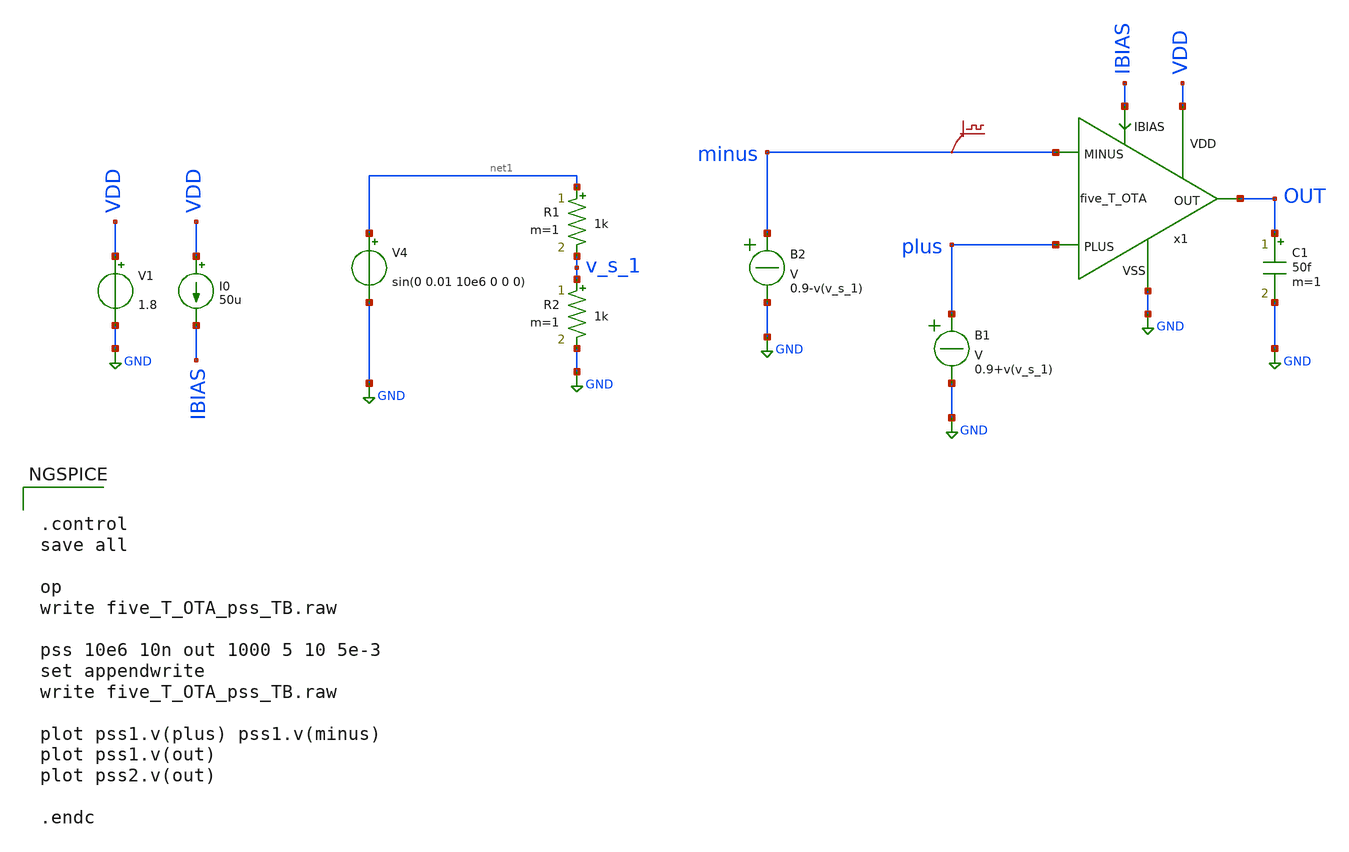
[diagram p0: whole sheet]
** sch_path: examples/xschem/five_T_OTA_pss_TB_2.sch
**.subckt five_T_OTA_pss_TB_2
x1 OUT minus plus IBIAS GND VDD five_T_OTA
V1 VDD GND 1.8
I0 VDD IBIAS 50u
C1 OUT GND 50f m=1
V4 net1 GND sin(0 0.01 10e6 0 0 0)
B1 plus GND V = 0.9+v(v_s_1)
R1 net1 v_s_1 1k m=1
R2 v_s_1 GND 1k m=1
B2 minus GND V = 0.9-v(v_s_1)
.save v(minus)
**** begin user architecture code


.control
save all

op
write five_T_OTA_pss_TB.raw

pss 10e6 10n out 1000 5 10 5e-3
set appendwrite
write five_T_OTA_pss_TB.raw

plot pss1.v(plus) pss1.v(minus)
plot pss1.v(out)
plot pss2.v(out)

.endc



** opencircuitdesign pdks install
.lib $::SKYWATER_MODELS/sky130.lib.spice tt


**** end user architecture code
**.ends

* expanding   symbol:  five_T_OTA.sym # of pins=6
** sym_path: examples/xschem/five_T_OTA.sym
** sch_path: examples/xschem/five_T_OTA.sch
.subckt five_T_OTA OUT MINUS PLUS IBIAS VSS VDD
*.iopin VDD
*.iopin VSS
*.iopin MINUS
*.iopin PLUS
*.iopin OUT
*.iopin IBIAS
XM2 IBIAS IBIAS VSS VSS sky130_fd_pr__nfet_01v8 L=0.3 W=3 nf=1 ad='int((nf+1)/2) * W/nf * 0.29' as='int((nf+2)/2) * W/nf * 0.29'
+ pd='2*int((nf+1)/2) * (W/nf + 0.29)' ps='2*int((nf+2)/2) * (W/nf + 0.29)' nrd='0.29 / W' nrs='0.29 / W'
+ sa=0 sb=0 sd=0 mult=1 m=1
XM1 net1 IBIAS VSS VSS sky130_fd_pr__nfet_01v8 L=0.3 W=3 nf=1 ad='int((nf+1)/2) * W/nf * 0.29' as='int((nf+2)/2) * W/nf * 0.29'
+ pd='2*int((nf+1)/2) * (W/nf + 0.29)' ps='2*int((nf+2)/2) * (W/nf + 0.29)' nrd='0.29 / W' nrs='0.29 / W'
+ sa=0 sb=0 sd=0 mult=4 m=4
.save v(ibias)
.save v(out)
.save v(net2)
.save v(net1)
XM4 net2 PLUS net1 VSS sky130_fd_pr__nfet_01v8_lvt L=0.3 W=4 nf=1 ad='int((nf+1)/2) * W/nf * 0.29' as='int((nf+2)/2) * W/nf * 0.29'
+ pd='2*int((nf+1)/2) * (W/nf + 0.29)' ps='2*int((nf+2)/2) * (W/nf + 0.29)' nrd='0.29 / W' nrs='0.29 / W'
+ sa=0 sb=0 sd=0 mult=4 m=4
XM5 OUT MINUS net1 VSS sky130_fd_pr__nfet_01v8_lvt L=0.3 W=4 nf=1 ad='int((nf+1)/2) * W/nf * 0.29' as='int((nf+2)/2) * W/nf * 0.29'
+ pd='2*int((nf+1)/2) * (W/nf + 0.29)' ps='2*int((nf+2)/2) * (W/nf + 0.29)' nrd='0.29 / W' nrs='0.29 / W'
+ sa=0 sb=0 sd=0 mult=4 m=4
XM3 net2 net2 VDD VDD sky130_fd_pr__pfet_01v8_lvt L=0.7 W=2.3 nf=1 ad='int((nf+1)/2) * W/nf * 0.29' as='int((nf+2)/2) * W/nf * 0.29'
+ pd='2*int((nf+1)/2) * (W/nf + 0.29)' ps='2*int((nf+2)/2) * (W/nf + 0.29)' nrd='0.29 / W' nrs='0.29 / W'
+ sa=0 sb=0 sd=0 mult=4 m=4
XM6 OUT net2 VDD VDD sky130_fd_pr__pfet_01v8_lvt L=0.7 W=2.3 nf=1 ad='int((nf+1)/2) * W/nf * 0.29' as='int((nf+2)/2) * W/nf * 0.29'
+ pd='2*int((nf+1)/2) * (W/nf + 0.29)' ps='2*int((nf+2)/2) * (W/nf + 0.29)' nrd='0.29 / W' nrs='0.29 / W'
+ sa=0 sb=0 sd=0 mult=4 m=4
.ends

.GLOBAL GND
.end
